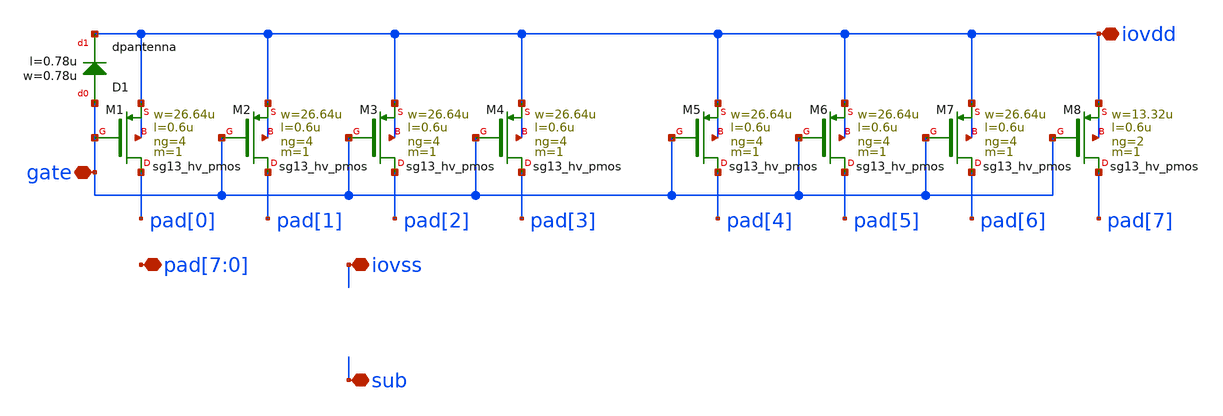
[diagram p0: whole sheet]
** sch_path: ihp-sg13g2/libs.tech/xschem/hm_stdcells/sg13g2_Clamp_P15N15D_noptap.sch
**.subckt sg13g2_Clamp_P15N15D_noptap iovss gate iovdd
*+ pad[7],pad[6],pad[5],pad[4],pad[3],pad[2],pad[1],pad[0] sub
*.iopin iovss
*.iopin gate
*.iopin iovdd
*.iopin pad[7],pad[6],pad[5],pad[4],pad[3],pad[2],pad[1],pad[0]
*.iopin sub
XM1 pad[0] gate iovdd iovdd sg13_hv_pmos w=26.64u l=0.6u ng=4 m=1 mm_ok=1
XD1 gate iovdd dpantenna l=0.78u w=0.78u
XM2 pad[1] gate iovdd iovdd sg13_hv_pmos w=26.64u l=0.6u ng=4 m=1 mm_ok=1
XM3 pad[2] gate iovdd iovdd sg13_hv_pmos w=26.64u l=0.6u ng=4 m=1 mm_ok=1
XM4 pad[3] gate iovdd iovdd sg13_hv_pmos w=26.64u l=0.6u ng=4 m=1 mm_ok=1
XM5 pad[4] gate iovdd iovdd sg13_hv_pmos w=26.64u l=0.6u ng=4 m=1 mm_ok=1
XM6 pad[5] gate iovdd iovdd sg13_hv_pmos w=26.64u l=0.6u ng=4 m=1 mm_ok=1
XM7 pad[6] gate iovdd iovdd sg13_hv_pmos w=26.64u l=0.6u ng=4 m=1 mm_ok=1
XM8 pad[7] gate iovdd iovdd sg13_hv_pmos w=13.32u l=0.6u ng=2 m=1 mm_ok=1
**.ends
.end
